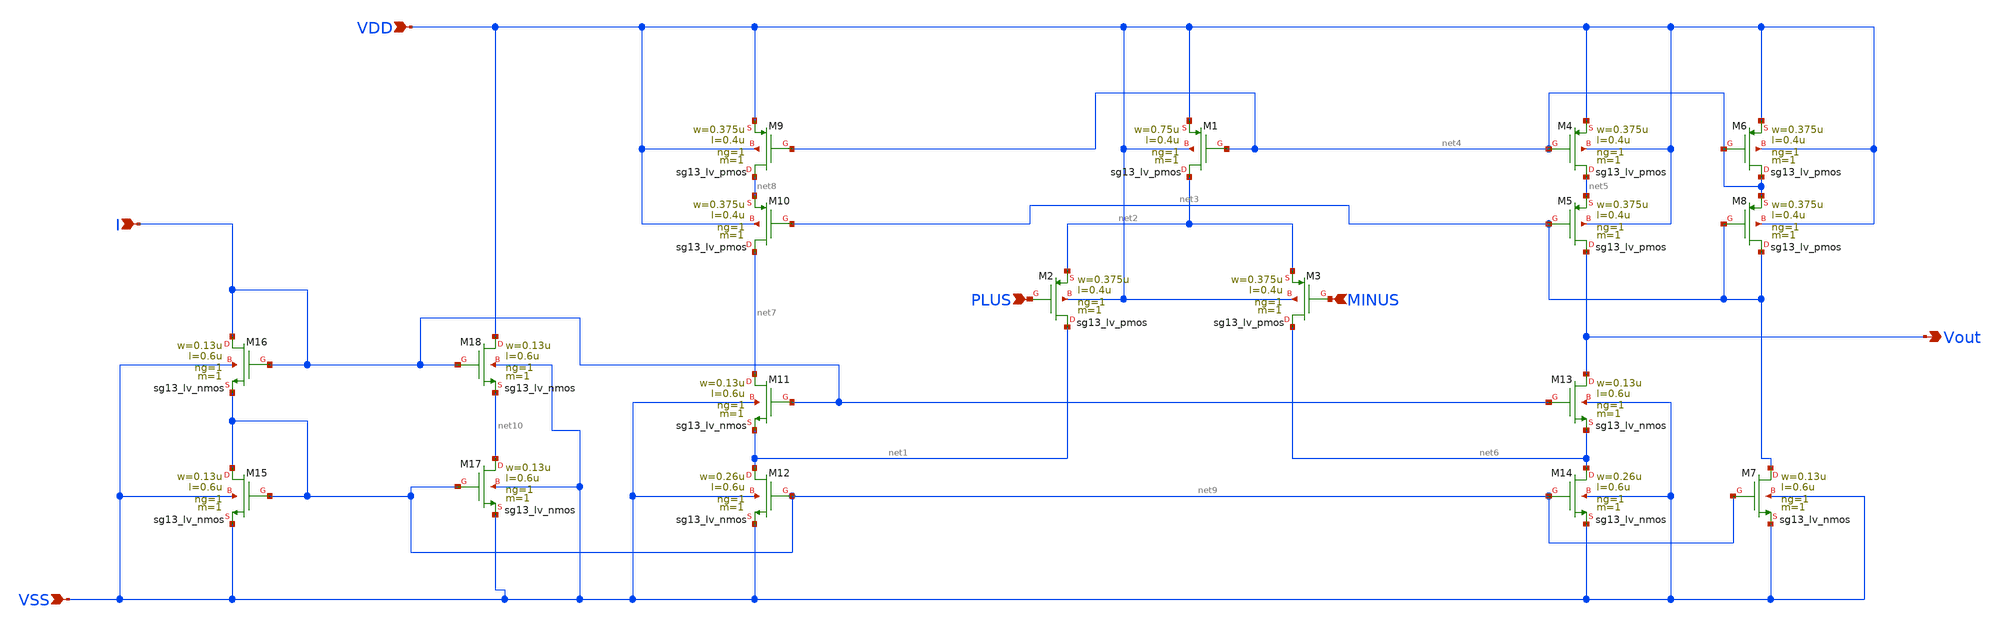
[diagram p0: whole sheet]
** sch_path: DSM/IC_Designs_Hrishi/RealCircuits/Folded Cascode/FoldedCascodeOTA.sch
* (c) 2024 Hrishikesh, @HSB
**.subckt FoldedCascodeOTA PLUS MINUS Vout VDD VSS I
*.ipin PLUS
*.ipin MINUS
*.opin Vout
*.ipin VDD
*.ipin VSS
*.ipin I
XM1 net2 net4 VDD VDD sg13_lv_pmos w=0.75u l=0.4u ng=1 m=1 mm_ok=1
XM2 net1 PLUS net2 VDD sg13_lv_pmos w=0.375u l=0.4u ng=1 m=1 mm_ok=1
XM3 net6 MINUS net2 VDD sg13_lv_pmos w=0.375u l=0.4u ng=1 m=1 mm_ok=1
XM14 net6 net9 VSS VSS sg13_lv_nmos w=0.26u l=0.6u ng=1 m=1 mm_ok=1
XM13 Vout I net6 VSS sg13_lv_nmos w=0.13u l=0.6u ng=1 m=1 mm_ok=1
XM11 net7 I net1 VSS sg13_lv_nmos w=0.13u l=0.6u ng=1 m=1 mm_ok=1
XM12 net1 net9 VSS VSS sg13_lv_nmos w=0.26u l=0.6u ng=1 m=1 mm_ok=1
XM9 net8 net4 VDD VDD sg13_lv_pmos w=0.375u l=0.4u ng=1 m=1 mm_ok=1
XM10 net7 net3 net8 VDD sg13_lv_pmos w=0.375u l=0.4u ng=1 m=1 mm_ok=1
XM4 net5 net4 VDD VDD sg13_lv_pmos w=0.375u l=0.4u ng=1 m=1 mm_ok=1
XM5 Vout net3 net5 VDD sg13_lv_pmos w=0.375u l=0.4u ng=1 m=1 mm_ok=1
XM6 net4 net4 VDD VDD sg13_lv_pmos w=0.375u l=0.4u ng=1 m=1 mm_ok=1
XM8 net3 net3 net4 VDD sg13_lv_pmos w=0.375u l=0.4u ng=1 m=1 mm_ok=1
XM7 net3 net9 VSS VSS sg13_lv_nmos w=0.13u l=0.6u ng=1 m=1 mm_ok=1
XM18 VDD I net10 VSS sg13_lv_nmos w=0.13u l=0.6u ng=1 m=1 mm_ok=1
XM17 net10 net9 VSS VSS sg13_lv_nmos w=0.13u l=0.6u ng=1 m=1 mm_ok=1
XM16 I I net9 VSS sg13_lv_nmos w=0.13u l=0.6u ng=1 m=1 mm_ok=1
XM15 net9 net9 VSS VSS sg13_lv_nmos w=0.13u l=0.6u ng=1 m=1 mm_ok=1
**.ends
.end
